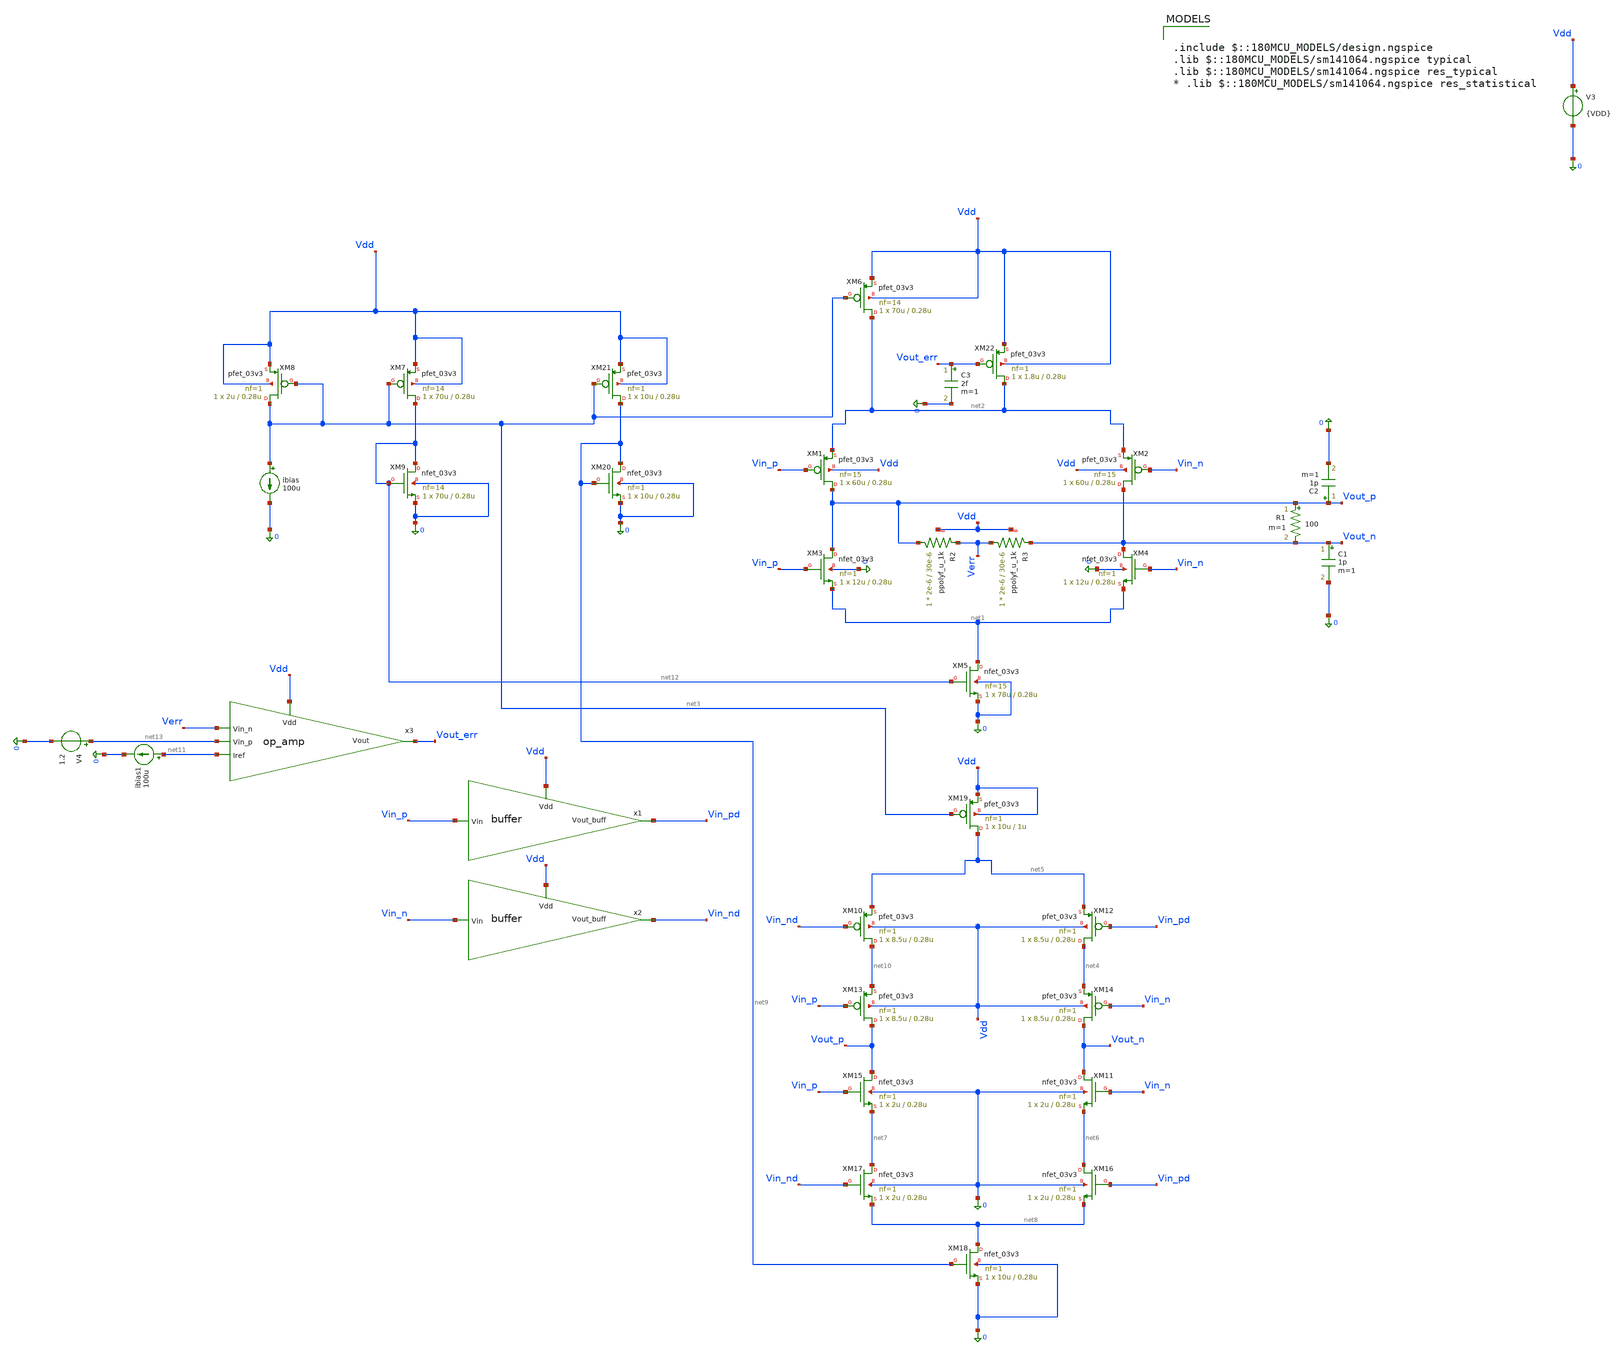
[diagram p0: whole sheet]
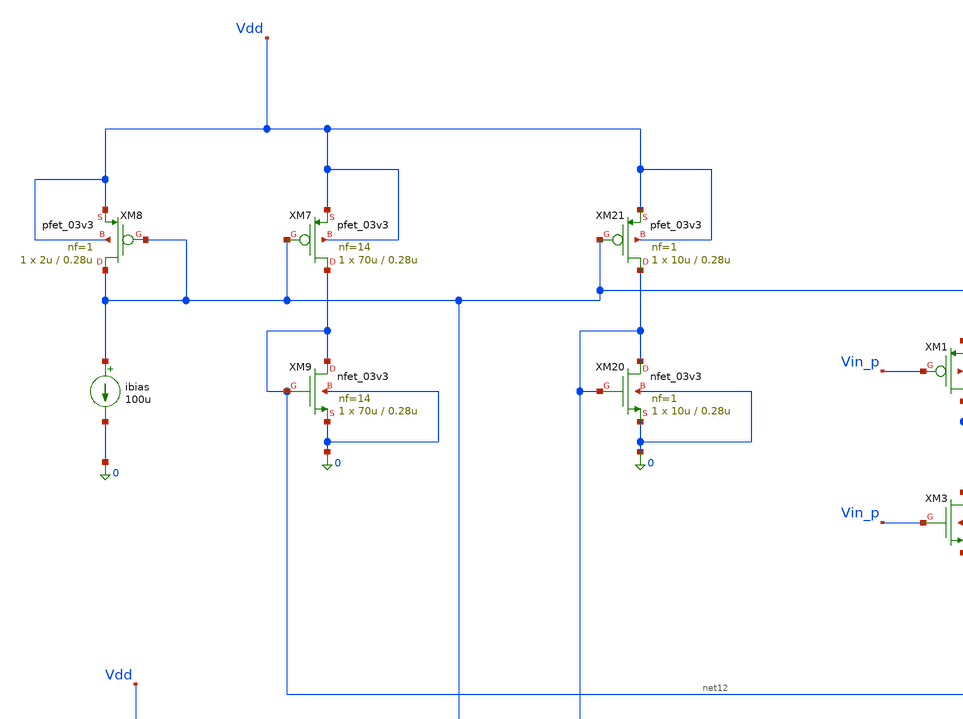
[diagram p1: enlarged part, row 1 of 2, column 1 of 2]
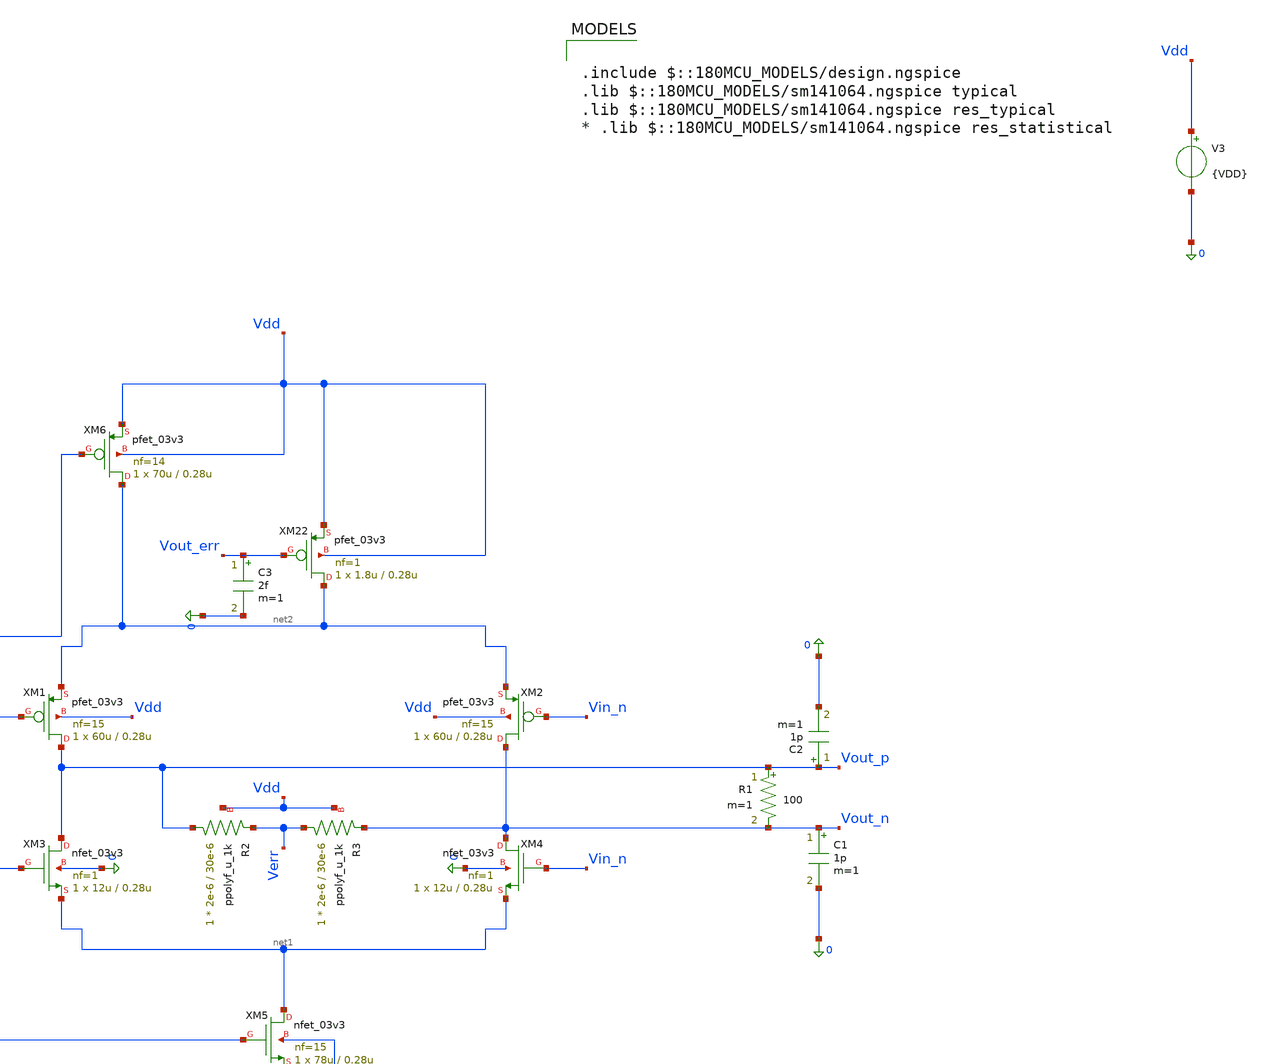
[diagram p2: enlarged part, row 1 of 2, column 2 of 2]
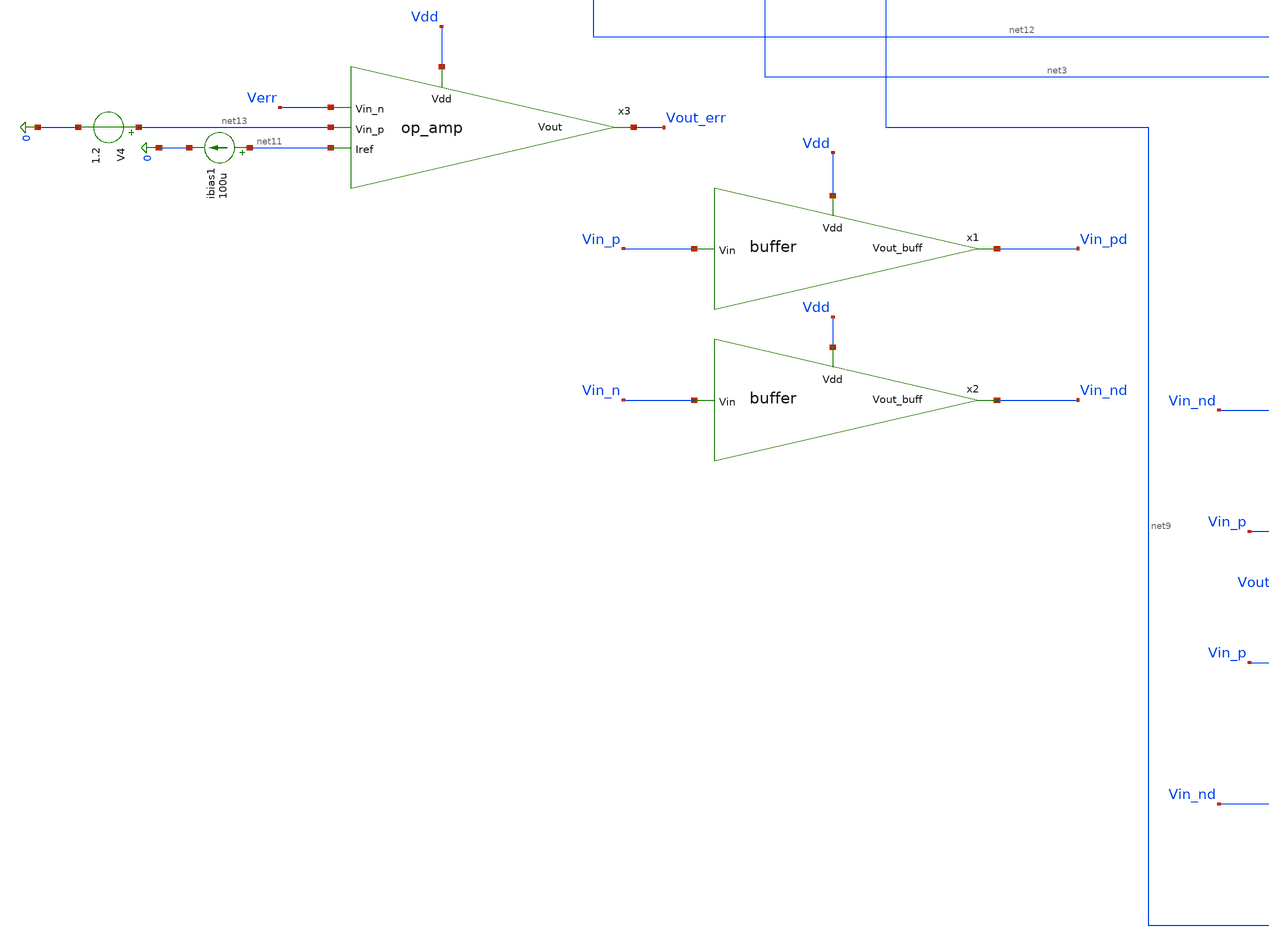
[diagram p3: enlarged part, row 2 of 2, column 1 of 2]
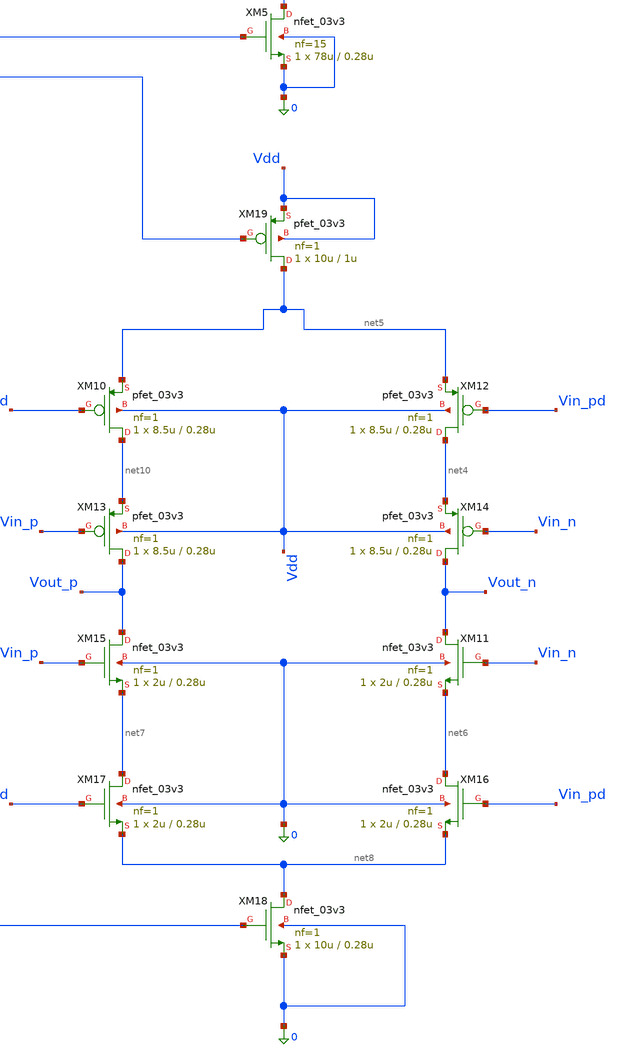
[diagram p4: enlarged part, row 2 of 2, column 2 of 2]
** sch_path: blocks/adc/lvds/lvds_testing.sch
**.subckt lvds_testing
R1 Vout_p Vout_n 100 m=1
V3 Vdd 0 {VDD}
XM1 Vout_p Vin_p net2 Vdd pfet_03v3 L=0.28u W=60u nf=15 ad='int((nf+1)/2) * W/nf * 0.18u' as='int((nf+2)/2) * W/nf * 0.18u'
+ pd='2*int((nf+1)/2) * (W/nf + 0.18u)' ps='2*int((nf+2)/2) * (W/nf + 0.18u)' nrd='0.18u / W' nrs='0.18u / W'
+ sa=0 sb=0 sd=0 m=1
XM2 Vout_n Vin_n net2 Vdd pfet_03v3 L=0.28u W=60u nf=15 ad='int((nf+1)/2) * W/nf * 0.18u' as='int((nf+2)/2) * W/nf * 0.18u'
+ pd='2*int((nf+1)/2) * (W/nf + 0.18u)' ps='2*int((nf+2)/2) * (W/nf + 0.18u)' nrd='0.18u / W' nrs='0.18u / W'
+ sa=0 sb=0 sd=0 m=1
XM3 Vout_p Vin_p net1 0 nfet_03v3 L=0.28u W=12u nf=1 ad='int((nf+1)/2) * W/nf * 0.18u' as='int((nf+2)/2) * W/nf * 0.18u'
+ pd='2*int((nf+1)/2) * (W/nf + 0.18u)' ps='2*int((nf+2)/2) * (W/nf + 0.18u)' nrd='0.18u / W' nrs='0.18u / W'
+ sa=0 sb=0 sd=0 m=1
XM4 Vout_n Vin_n net1 0 nfet_03v3 L=0.28u W=12u nf=1 ad='int((nf+1)/2) * W/nf * 0.18u' as='int((nf+2)/2) * W/nf * 0.18u'
+ pd='2*int((nf+1)/2) * (W/nf + 0.18u)' ps='2*int((nf+2)/2) * (W/nf + 0.18u)' nrd='0.18u / W' nrs='0.18u / W'
+ sa=0 sb=0 sd=0 m=1
XM5 net1 net12 0 0 nfet_03v3 L=0.28u W=78u nf=15 ad='int((nf+1)/2) * W/nf * 0.18u' as='int((nf+2)/2) * W/nf * 0.18u'
+ pd='2*int((nf+1)/2) * (W/nf + 0.18u)' ps='2*int((nf+2)/2) * (W/nf + 0.18u)' nrd='0.18u / W' nrs='0.18u / W'
+ sa=0 sb=0 sd=0 m=1
XM6 net2 net3 Vdd Vdd pfet_03v3 L=0.28u W=70u nf=14 ad='int((nf+1)/2) * W/nf * 0.18u' as='int((nf+2)/2) * W/nf * 0.18u'
+ pd='2*int((nf+1)/2) * (W/nf + 0.18u)' ps='2*int((nf+2)/2) * (W/nf + 0.18u)' nrd='0.18u / W' nrs='0.18u / W'
+ sa=0 sb=0 sd=0 m=1
XM8 net3 net3 Vdd Vdd pfet_03v3 L=0.28u W=2u nf=1 ad='int((nf+1)/2) * W/nf * 0.18u' as='int((nf+2)/2) * W/nf * 0.18u'
+ pd='2*int((nf+1)/2) * (W/nf + 0.18u)' ps='2*int((nf+2)/2) * (W/nf + 0.18u)' nrd='0.18u / W' nrs='0.18u / W'
+ sa=0 sb=0 sd=0 m=1
ibias net3 0 100u
XM10 net10 Vin_nd net5 Vdd pfet_03v3 L=0.28u W=8.5u nf=1 ad='int((nf+1)/2) * W/nf * 0.18u' as='int((nf+2)/2) * W/nf * 0.18u'
+ pd='2*int((nf+1)/2) * (W/nf + 0.18u)' ps='2*int((nf+2)/2) * (W/nf + 0.18u)' nrd='0.18u / W' nrs='0.18u / W'
+ sa=0 sb=0 sd=0 m=1
XM11 Vout_n Vin_n net6 0 nfet_03v3 L=0.28u W=2u nf=1 ad='int((nf+1)/2) * W/nf * 0.18u' as='int((nf+2)/2) * W/nf * 0.18u'
+ pd='2*int((nf+1)/2) * (W/nf + 0.18u)' ps='2*int((nf+2)/2) * (W/nf + 0.18u)' nrd='0.18u / W' nrs='0.18u / W'
+ sa=0 sb=0 sd=0 m=1
XM12 net4 Vin_pd net5 Vdd pfet_03v3 L=0.28u W=8.5u nf=1 ad='int((nf+1)/2) * W/nf * 0.18u' as='int((nf+2)/2) * W/nf * 0.18u'
+ pd='2*int((nf+1)/2) * (W/nf + 0.18u)' ps='2*int((nf+2)/2) * (W/nf + 0.18u)' nrd='0.18u / W' nrs='0.18u / W'
+ sa=0 sb=0 sd=0 m=1
XM13 Vout_p Vin_p net10 Vdd pfet_03v3 L=0.28u W=8.5u nf=1 ad='int((nf+1)/2) * W/nf * 0.18u' as='int((nf+2)/2) * W/nf * 0.18u'
+ pd='2*int((nf+1)/2) * (W/nf + 0.18u)' ps='2*int((nf+2)/2) * (W/nf + 0.18u)' nrd='0.18u / W' nrs='0.18u / W'
+ sa=0 sb=0 sd=0 m=1
XM14 Vout_n Vin_n net4 Vdd pfet_03v3 L=0.28u W=8.5u nf=1 ad='int((nf+1)/2) * W/nf * 0.18u' as='int((nf+2)/2) * W/nf * 0.18u'
+ pd='2*int((nf+1)/2) * (W/nf + 0.18u)' ps='2*int((nf+2)/2) * (W/nf + 0.18u)' nrd='0.18u / W' nrs='0.18u / W'
+ sa=0 sb=0 sd=0 m=1
XM15 Vout_p Vin_p net7 0 nfet_03v3 L=0.28u W=2u nf=1 ad='int((nf+1)/2) * W/nf * 0.18u' as='int((nf+2)/2) * W/nf * 0.18u'
+ pd='2*int((nf+1)/2) * (W/nf + 0.18u)' ps='2*int((nf+2)/2) * (W/nf + 0.18u)' nrd='0.18u / W' nrs='0.18u / W'
+ sa=0 sb=0 sd=0 m=1
XM16 net6 Vin_pd net8 0 nfet_03v3 L=0.28u W=2u nf=1 ad='int((nf+1)/2) * W/nf * 0.18u' as='int((nf+2)/2) * W/nf * 0.18u'
+ pd='2*int((nf+1)/2) * (W/nf + 0.18u)' ps='2*int((nf+2)/2) * (W/nf + 0.18u)' nrd='0.18u / W' nrs='0.18u / W'
+ sa=0 sb=0 sd=0 m=1
XM17 net7 Vin_nd net8 0 nfet_03v3 L=0.28u W=2u nf=1 ad='int((nf+1)/2) * W/nf * 0.18u' as='int((nf+2)/2) * W/nf * 0.18u'
+ pd='2*int((nf+1)/2) * (W/nf + 0.18u)' ps='2*int((nf+2)/2) * (W/nf + 0.18u)' nrd='0.18u / W' nrs='0.18u / W'
+ sa=0 sb=0 sd=0 m=1
XM18 net8 net9 0 0 nfet_03v3 L=0.28u W=10u nf=1 ad='int((nf+1)/2) * W/nf * 0.18u' as='int((nf+2)/2) * W/nf * 0.18u'
+ pd='2*int((nf+1)/2) * (W/nf + 0.18u)' ps='2*int((nf+2)/2) * (W/nf + 0.18u)' nrd='0.18u / W' nrs='0.18u / W'
+ sa=0 sb=0 sd=0 m=1
XM19 net5 net3 Vdd Vdd pfet_03v3 L=1u W=10u nf=1 ad='int((nf+1)/2) * W/nf * 0.18u' as='int((nf+2)/2) * W/nf * 0.18u'
+ pd='2*int((nf+1)/2) * (W/nf + 0.18u)' ps='2*int((nf+2)/2) * (W/nf + 0.18u)' nrd='0.18u / W' nrs='0.18u / W'
+ sa=0 sb=0 sd=0 m=1
x1 Vdd Vin_pd Vin_p buffer
x2 Vdd Vin_nd Vin_n buffer
XM21 net9 net3 Vdd Vdd pfet_03v3 L=0.28u W=10u nf=1 ad='int((nf+1)/2) * W/nf * 0.18u' as='int((nf+2)/2) * W/nf * 0.18u'
+ pd='2*int((nf+1)/2) * (W/nf + 0.18u)' ps='2*int((nf+2)/2) * (W/nf + 0.18u)' nrd='0.18u / W' nrs='0.18u / W'
+ sa=0 sb=0 sd=0 m=1
XM20 net9 net9 0 0 nfet_03v3 L=0.28u W=10u nf=1 ad='int((nf+1)/2) * W/nf * 0.18u' as='int((nf+2)/2) * W/nf * 0.18u'
+ pd='2*int((nf+1)/2) * (W/nf + 0.18u)' ps='2*int((nf+2)/2) * (W/nf + 0.18u)' nrd='0.18u / W' nrs='0.18u / W'
+ sa=0 sb=0 sd=0 m=1
C2 Vout_p 0 1p m=1
XR2 Vout_p Verr Vdd ppolyf_u_1k r_width=2e-6 r_length=30e-6 m=1
XR3 Verr Vout_n Vdd ppolyf_u_1k r_width=2e-6 r_length=30e-6 m=1
ibias1 net11 0 100u
V4 net13 0 1.2
XM7 net12 net3 Vdd Vdd pfet_03v3 L=0.28u W=70u nf=14 ad='int((nf+1)/2) * W/nf * 0.18u' as='int((nf+2)/2) * W/nf * 0.18u'
+ pd='2*int((nf+1)/2) * (W/nf + 0.18u)' ps='2*int((nf+2)/2) * (W/nf + 0.18u)' nrd='0.18u / W' nrs='0.18u / W'
+ sa=0 sb=0 sd=0 m=1
XM9 net12 net12 0 0 nfet_03v3 L=0.28u W=70u nf=14 ad='int((nf+1)/2) * W/nf * 0.18u' as='int((nf+2)/2) * W/nf * 0.18u'
+ pd='2*int((nf+1)/2) * (W/nf + 0.18u)' ps='2*int((nf+2)/2) * (W/nf + 0.18u)' nrd='0.18u / W' nrs='0.18u / W'
+ sa=0 sb=0 sd=0 m=1
C1 Vout_n 0 1p m=1
XM22 net2 Vout_err Vdd Vdd pfet_03v3 L=0.28u W=1.8u nf=1 ad='int((nf+1)/2) * W/nf * 0.18u' as='int((nf+2)/2) * W/nf * 0.18u'
+ pd='2*int((nf+1)/2) * (W/nf + 0.18u)' ps='2*int((nf+2)/2) * (W/nf + 0.18u)' nrd='0.18u / W' nrs='0.18u / W'
+ sa=0 sb=0 sd=0 m=1
x3 Vdd Vout_err Verr net13 net11 op_amp
C3 Vout_err 0 2f m=1
**** begin user architecture code


.options temp=27

.param VDD=3.3
.param VCM=1.2

* 2 Gbps data rate
.param UI=500p
.param TR=20p
.param SEED=11

* Input timing jitter, peak-to-peak
* Set TJPP=0p for no jitter
.param TJPP=40p

* ============================================================
* Internal pseudo-random data generation with shared edge jitter
* ============================================================
.func frac(x) {x - floor(x)}

.func rand01(n) {frac(sin((n + 1 + SEED)*12.9898)*43758.5453123)}
.func rand01j(n) {frac(sin((n + 1 + SEED)*78.233)*24634.6345)}

.func rbit(n) {floor(2*rand01(n))}
.func jitter(n) {(rand01j(n)-0.5)*TJPP}

.func edge(x) {0.5*(1 + tanh(x/(TR/10)))}

.func data_bit(t) {rbit(floor(t/UI)-1)+(rbit(floor(t/UI))-rbit(floor(t/UI)-1))*edge(t-floor(t/UI)*UI-jitter(floor(t/UI)))}

* ============================================================
* Behavioral input sources
*
* IMPORTANT:
* Delete/disable any schematic PULSE or bsource symbols
* connected to vin_p / vin_n when using these.
* ============================================================

Bvinp vin_p 0 V={VDD*data_bit(time)}
Bvinn vin_n 0 V={VDD*(1 - data_bit(time))}

.control
set filetype=ascii
set wr_singlescale
set numdgt=12

shell rm /foss/designs/trans_testing/lvds_testing/lvds_eye_temp_27.txt

save v(vin_p) v(vin_n) v(vout_p) v(vout_n)

tran 2p 200n 0 2p

let vod = v(vout_p)-v(vout_n)
let vcm_out = (v(vout_p)+v(vout_n))/2
let vod_abs = abs(vod)

meas tran vcm_avg avg vcm_out from=20n to=200n
meas tran vcm_max max vcm_out from=20n to=200n
meas tran vcm_min min vcm_out from=20n to=200n

meas tran vod_abs_avg avg vod_abs from=20n to=200n
meas tran vod_max max vod from=20n to=200n
meas tran vod_min min vod from=20n to=200n

wrdata /foss/designs/trans_testing/lvds_testing/lvds_eye_temp_27.txt v(vin_p) v(vin_n) v(vout_p)
+ v(vout_n) vod vcm_out

.endc



.include $::180MCU_MODELS/design.ngspice
.lib $::180MCU_MODELS/sm141064.ngspice typical
.lib $::180MCU_MODELS/sm141064.ngspice res_typical
* .lib $::180MCU_MODELS/sm141064.ngspice res_statistical

**** end user architecture code
**.ends

* expanding   symbol:  buffer.sym # of pins=3
** sym_path: blocks/adc/lvds/buffer.sym
** sch_path: blocks/adc/lvds/buffer.sch
.subckt buffer Vdd Vout_buff Vin
*.ipin Vdd
*.ipin Vin
*.opin Vout_buff
XM1 net1 Vin Vdd Vdd pfet_03v3 L=0.28u W=0.66u nf=1 ad='int((nf+1)/2) * W/nf * 0.18u' as='int((nf+2)/2) * W/nf * 0.18u'
+ pd='2*int((nf+1)/2) * (W/nf + 0.18u)' ps='2*int((nf+2)/2) * (W/nf + 0.18u)' nrd='0.18u / W' nrs='0.18u / W'
+ sa=0 sb=0 sd=0 m=1
XM2 net1 Vin 0 0 nfet_03v3 L=0.28u W=0.22u nf=1 ad='int((nf+1)/2) * W/nf * 0.18u' as='int((nf+2)/2) * W/nf * 0.18u'
+ pd='2*int((nf+1)/2) * (W/nf + 0.18u)' ps='2*int((nf+2)/2) * (W/nf + 0.18u)' nrd='0.18u / W' nrs='0.18u / W'
+ sa=0 sb=0 sd=0 m=1
XM3 net2 net1 Vdd Vdd pfet_03v3 L=0.28u W=2.64u nf=1 ad='int((nf+1)/2) * W/nf * 0.18u' as='int((nf+2)/2) * W/nf * 0.18u'
+ pd='2*int((nf+1)/2) * (W/nf + 0.18u)' ps='2*int((nf+2)/2) * (W/nf + 0.18u)' nrd='0.18u / W' nrs='0.18u / W'
+ sa=0 sb=0 sd=0 m=1
XM4 net2 net1 0 0 nfet_03v3 L=0.28u W=0.88u nf=1 ad='int((nf+1)/2) * W/nf * 0.18u' as='int((nf+2)/2) * W/nf * 0.18u'
+ pd='2*int((nf+1)/2) * (W/nf + 0.18u)' ps='2*int((nf+2)/2) * (W/nf + 0.18u)' nrd='0.18u / W' nrs='0.18u / W'
+ sa=0 sb=0 sd=0 m=1
XM5 net3 net2 Vdd Vdd pfet_03v3 L=0.28u W=10.56u nf=1 ad='int((nf+1)/2) * W/nf * 0.18u' as='int((nf+2)/2) * W/nf * 0.18u'
+ pd='2*int((nf+1)/2) * (W/nf + 0.18u)' ps='2*int((nf+2)/2) * (W/nf + 0.18u)' nrd='0.18u / W' nrs='0.18u / W'
+ sa=0 sb=0 sd=0 m=1
XM6 net3 net2 0 0 nfet_03v3 L=0.28u W=3.52u nf=1 ad='int((nf+1)/2) * W/nf * 0.18u' as='int((nf+2)/2) * W/nf * 0.18u'
+ pd='2*int((nf+1)/2) * (W/nf + 0.18u)' ps='2*int((nf+2)/2) * (W/nf + 0.18u)' nrd='0.18u / W' nrs='0.18u / W'
+ sa=0 sb=0 sd=0 m=1
XM7 Vout_buff net3 Vdd Vdd pfet_03v3 L=0.28u W=42.24u nf=1 ad='int((nf+1)/2) * W/nf * 0.18u' as='int((nf+2)/2) * W/nf * 0.18u'
+ pd='2*int((nf+1)/2) * (W/nf + 0.18u)' ps='2*int((nf+2)/2) * (W/nf + 0.18u)' nrd='0.18u / W' nrs='0.18u / W'
+ sa=0 sb=0 sd=0 m=1
XM8 Vout_buff net3 0 0 nfet_03v3 L=0.28u W=14.08u nf=1 ad='int((nf+1)/2) * W/nf * 0.18u' as='int((nf+2)/2) * W/nf * 0.18u'
+ pd='2*int((nf+1)/2) * (W/nf + 0.18u)' ps='2*int((nf+2)/2) * (W/nf + 0.18u)' nrd='0.18u / W' nrs='0.18u / W'
+ sa=0 sb=0 sd=0 m=1
.ends


* expanding   symbol:  op_amp.sym # of pins=5
** sym_path: blocks/adc/lvds/op_amp.sym
** sch_path: blocks/adc/lvds/op_amp.sch
.subckt op_amp Vdd Vout Vin_n Vin_p Iref
*.ipin Vdd
*.ipin Vin_p
*.ipin Vin_n
*.opin Vout
*.ipin Iref
XM1 net2 net3 Vdd Vdd pfet_03v3 L=0.28u W=10.5u nf=1 ad='int((nf+1)/2) * W/nf * 0.18u' as='int((nf+2)/2) * W/nf * 0.18u'
+ pd='2*int((nf+1)/2) * (W/nf + 0.18u)' ps='2*int((nf+2)/2) * (W/nf + 0.18u)' nrd='0.18u / W' nrs='0.18u / W'
+ sa=0 sb=0 sd=0 m=1
XM2 net1 net4 Vdd Vdd pfet_03v3 L=0.28u W=10.5u nf=1 ad='int((nf+1)/2) * W/nf * 0.18u' as='int((nf+2)/2) * W/nf * 0.18u'
+ pd='2*int((nf+1)/2) * (W/nf + 0.18u)' ps='2*int((nf+2)/2) * (W/nf + 0.18u)' nrd='0.18u / W' nrs='0.18u / W'
+ sa=0 sb=0 sd=0 m=1
XM3 net3 Vb2 net2 Vdd pfet_03v3 L=0.28u W=10.5u nf=1 ad='int((nf+1)/2) * W/nf * 0.18u' as='int((nf+2)/2) * W/nf * 0.18u'
+ pd='2*int((nf+1)/2) * (W/nf + 0.18u)' ps='2*int((nf+2)/2) * (W/nf + 0.18u)' nrd='0.18u / W' nrs='0.18u / W'
+ sa=0 sb=0 sd=0 m=1
XM4 net4 Vb2 net1 Vdd pfet_03v3 L=0.28u W=10.5u nf=1 ad='int((nf+1)/2) * W/nf * 0.18u' as='int((nf+2)/2) * W/nf * 0.18u'
+ pd='2*int((nf+1)/2) * (W/nf + 0.18u)' ps='2*int((nf+2)/2) * (W/nf + 0.18u)' nrd='0.18u / W' nrs='0.18u / W'
+ sa=0 sb=0 sd=0 m=1
XM5 net4 Vin_p net5 0 nfet_03v3 L=0.28u W=52.5u nf=15 ad='int((nf+1)/2) * W/nf * 0.18u' as='int((nf+2)/2) * W/nf * 0.18u'
+ pd='2*int((nf+1)/2) * (W/nf + 0.18u)' ps='2*int((nf+2)/2) * (W/nf + 0.18u)' nrd='0.18u / W' nrs='0.18u / W'
+ sa=0 sb=0 sd=0 m=1
XM6 net3 Vin_n net5 0 nfet_03v3 L=0.28u W=52.5u nf=15 ad='int((nf+1)/2) * W/nf * 0.18u' as='int((nf+2)/2) * W/nf * 0.18u'
+ pd='2*int((nf+1)/2) * (W/nf + 0.18u)' ps='2*int((nf+2)/2) * (W/nf + 0.18u)' nrd='0.18u / W' nrs='0.18u / W'
+ sa=0 sb=0 sd=0 m=1
XM7 net6 net4 Vdd Vdd pfet_03v3 L=0.28u W=10.5u nf=1 ad='int((nf+1)/2) * W/nf * 0.18u' as='int((nf+2)/2) * W/nf * 0.18u'
+ pd='2*int((nf+1)/2) * (W/nf + 0.18u)' ps='2*int((nf+2)/2) * (W/nf + 0.18u)' nrd='0.18u / W' nrs='0.18u / W'
+ sa=0 sb=0 sd=0 m=1
XM9 net7 net3 Vdd Vdd pfet_03v3 L=0.28u W=10.5u nf=1 ad='int((nf+1)/2) * W/nf * 0.18u' as='int((nf+2)/2) * W/nf * 0.18u'
+ pd='2*int((nf+1)/2) * (W/nf + 0.18u)' ps='2*int((nf+2)/2) * (W/nf + 0.18u)' nrd='0.18u / W' nrs='0.18u / W'
+ sa=0 sb=0 sd=0 m=1
XM11 net8 Vb2 net10 0 nfet_03v3 L=0.28u W=5.25u nf=1 ad='int((nf+1)/2) * W/nf * 0.18u' as='int((nf+2)/2) * W/nf * 0.18u'
+ pd='2*int((nf+1)/2) * (W/nf + 0.18u)' ps='2*int((nf+2)/2) * (W/nf + 0.18u)' nrd='0.18u / W' nrs='0.18u / W'
+ sa=0 sb=0 sd=0 m=1
XM12 Vout Vb2 net9 0 nfet_03v3 L=0.28u W=5.25u nf=1 ad='int((nf+1)/2) * W/nf * 0.18u' as='int((nf+2)/2) * W/nf * 0.18u'
+ pd='2*int((nf+1)/2) * (W/nf + 0.18u)' ps='2*int((nf+2)/2) * (W/nf + 0.18u)' nrd='0.18u / W' nrs='0.18u / W'
+ sa=0 sb=0 sd=0 m=1
XM13 net10 net8 0 0 nfet_03v3 L=0.28u W=5.25u nf=1 ad='int((nf+1)/2) * W/nf * 0.18u' as='int((nf+2)/2) * W/nf * 0.18u'
+ pd='2*int((nf+1)/2) * (W/nf + 0.18u)' ps='2*int((nf+2)/2) * (W/nf + 0.18u)' nrd='0.18u / W' nrs='0.18u / W'
+ sa=0 sb=0 sd=0 m=1
XM14 net9 net8 0 0 nfet_03v3 L=0.28u W=5.25u nf=1 ad='int((nf+1)/2) * W/nf * 0.18u' as='int((nf+2)/2) * W/nf * 0.18u'
+ pd='2*int((nf+1)/2) * (W/nf + 0.18u)' ps='2*int((nf+2)/2) * (W/nf + 0.18u)' nrd='0.18u / W' nrs='0.18u / W'
+ sa=0 sb=0 sd=0 m=1
XM8 net8 0 net6 Vdd pfet_03v3 L=0.28u W=10.5u nf=1 ad='int((nf+1)/2) * W/nf * 0.18u' as='int((nf+2)/2) * W/nf * 0.18u'
+ pd='2*int((nf+1)/2) * (W/nf + 0.18u)' ps='2*int((nf+2)/2) * (W/nf + 0.18u)' nrd='0.18u / W' nrs='0.18u / W'
+ sa=0 sb=0 sd=0 m=1
XM10 Vout 0 net7 Vdd pfet_03v3 L=0.28u W=10.5u nf=1 ad='int((nf+1)/2) * W/nf * 0.18u' as='int((nf+2)/2) * W/nf * 0.18u'
+ pd='2*int((nf+1)/2) * (W/nf + 0.18u)' ps='2*int((nf+2)/2) * (W/nf + 0.18u)' nrd='0.18u / W' nrs='0.18u / W'
+ sa=0 sb=0 sd=0 m=1
XM15 net5 net11 0 0 nfet_03v3 L=1u W=80u nf=20 ad='int((nf+1)/2) * W/nf * 0.18u' as='int((nf+2)/2) * W/nf * 0.18u'
+ pd='2*int((nf+1)/2) * (W/nf + 0.18u)' ps='2*int((nf+2)/2) * (W/nf + 0.18u)' nrd='0.18u / W' nrs='0.18u / W'
+ sa=0 sb=0 sd=0 m=1
XM16 Iref Iref Vdd Vdd pfet_03v3 L=1u W=20u nf=1 ad='int((nf+1)/2) * W/nf * 0.18u' as='int((nf+2)/2) * W/nf * 0.18u'
+ pd='2*int((nf+1)/2) * (W/nf + 0.18u)' ps='2*int((nf+2)/2) * (W/nf + 0.18u)' nrd='0.18u / W' nrs='0.18u / W'
+ sa=0 sb=0 sd=0 m=1
XM17 net11 Iref Vdd Vdd pfet_03v3 L=1u W=80u nf=1 ad='int((nf+1)/2) * W/nf * 0.18u' as='int((nf+2)/2) * W/nf * 0.18u'
+ pd='2*int((nf+1)/2) * (W/nf + 0.18u)' ps='2*int((nf+2)/2) * (W/nf + 0.18u)' nrd='0.18u / W' nrs='0.18u / W'
+ sa=0 sb=0 sd=0 m=1
XM18 Vb2 Iref Vdd Vdd pfet_03v3 L=1u W=20u nf=1 ad='int((nf+1)/2) * W/nf * 0.18u' as='int((nf+2)/2) * W/nf * 0.18u'
+ pd='2*int((nf+1)/2) * (W/nf + 0.18u)' ps='2*int((nf+2)/2) * (W/nf + 0.18u)' nrd='0.18u / W' nrs='0.18u / W'
+ sa=0 sb=0 sd=0 m=1
XM19 Vb2 Vb2 net12 0 nfet_03v3 L=0.28u W=30u nf=1 ad='int((nf+1)/2) * W/nf * 0.18u' as='int((nf+2)/2) * W/nf * 0.18u'
+ pd='2*int((nf+1)/2) * (W/nf + 0.18u)' ps='2*int((nf+2)/2) * (W/nf + 0.18u)' nrd='0.18u / W' nrs='0.18u / W'
+ sa=0 sb=0 sd=0 m=1
XM20 net12 net12 0 0 nfet_03v3 L=0.28u W=30u nf=1 ad='int((nf+1)/2) * W/nf * 0.18u' as='int((nf+2)/2) * W/nf * 0.18u'
+ pd='2*int((nf+1)/2) * (W/nf + 0.18u)' ps='2*int((nf+2)/2) * (W/nf + 0.18u)' nrd='0.18u / W' nrs='0.18u / W'
+ sa=0 sb=0 sd=0 m=1
XM21 net11 net11 0 0 nfet_03v3 L=1u W=80u nf=1 ad='int((nf+1)/2) * W/nf * 0.18u' as='int((nf+2)/2) * W/nf * 0.18u'
+ pd='2*int((nf+1)/2) * (W/nf + 0.18u)' ps='2*int((nf+2)/2) * (W/nf + 0.18u)' nrd='0.18u / W' nrs='0.18u / W'
+ sa=0 sb=0 sd=0 m=1
.ends

.end
